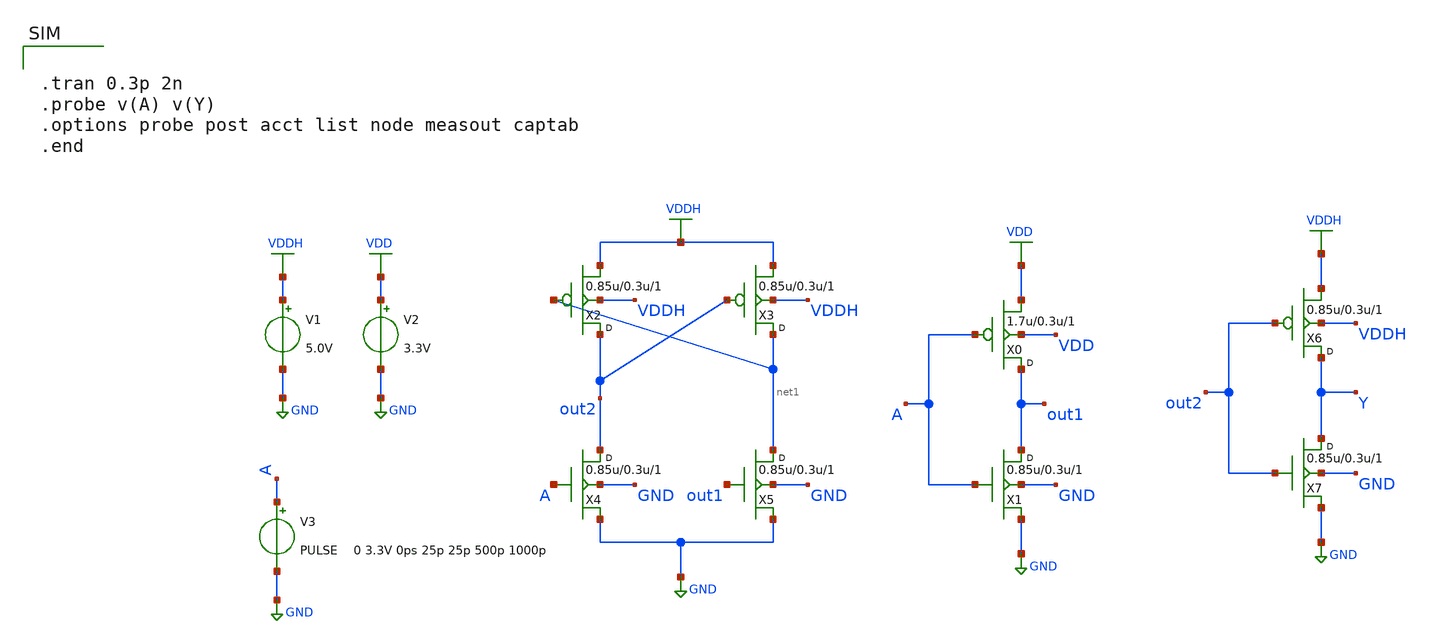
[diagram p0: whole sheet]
** sch_path: gf180mcu_osu_sc_gp12t3v3/cells/lshifup/gf180mcu_osu_sc_gp12t3v3__lshifup.sch
**.subckt gf180mcu_osu_sc_gp12t3v3__lshifup
X0 out1 A VDD VDD pfet_03p3 w=1.7u l=0.3u m=1
X1 out1 A GND GND nfet_03p3 w=0.85u l=0.3u m=1
X2 out2 net1 VDDH VDDH pfet_03p3 w=0.85u l=0.3u m=1
X3 net1 out2 VDDH VDDH pfet_03p3 w=0.85u l=0.3u m=1
X4 out2 A GND GND nfet_03p3 w=0.85u l=0.3u m=1
X5 net1 out1 GND GND nfet_03p3 w=0.85u l=0.3u m=1
X6 Y out2 VDDH VDDH pfet_03p3 w=0.85u l=0.3u m=1
X7 Y out2 GND GND nfet_03p3 w=0.85u l=0.3u m=1
V1 VDDH GND 5.0V
V2 VDD GND 3.3V
V3 A GND PULSE 0 3.3V 0ps 25p 25p 500p 1000p
**** begin user architecture code

.temp 25
.inc "/import/yukari1/lrburle/OSU_180/char/techfiles/design.hspice"
.lib "/import/yukari1/lrburle/OSU_180/char/techfiles/sm141064.hspice" typical



.tran 0.3p 2n
.probe v(A) v(Y)
.options probe post acct list node measout captab
.end


**** end user architecture code
**.ends
.GLOBAL VDD
.GLOBAL GND
.GLOBAL VDDH
.end
